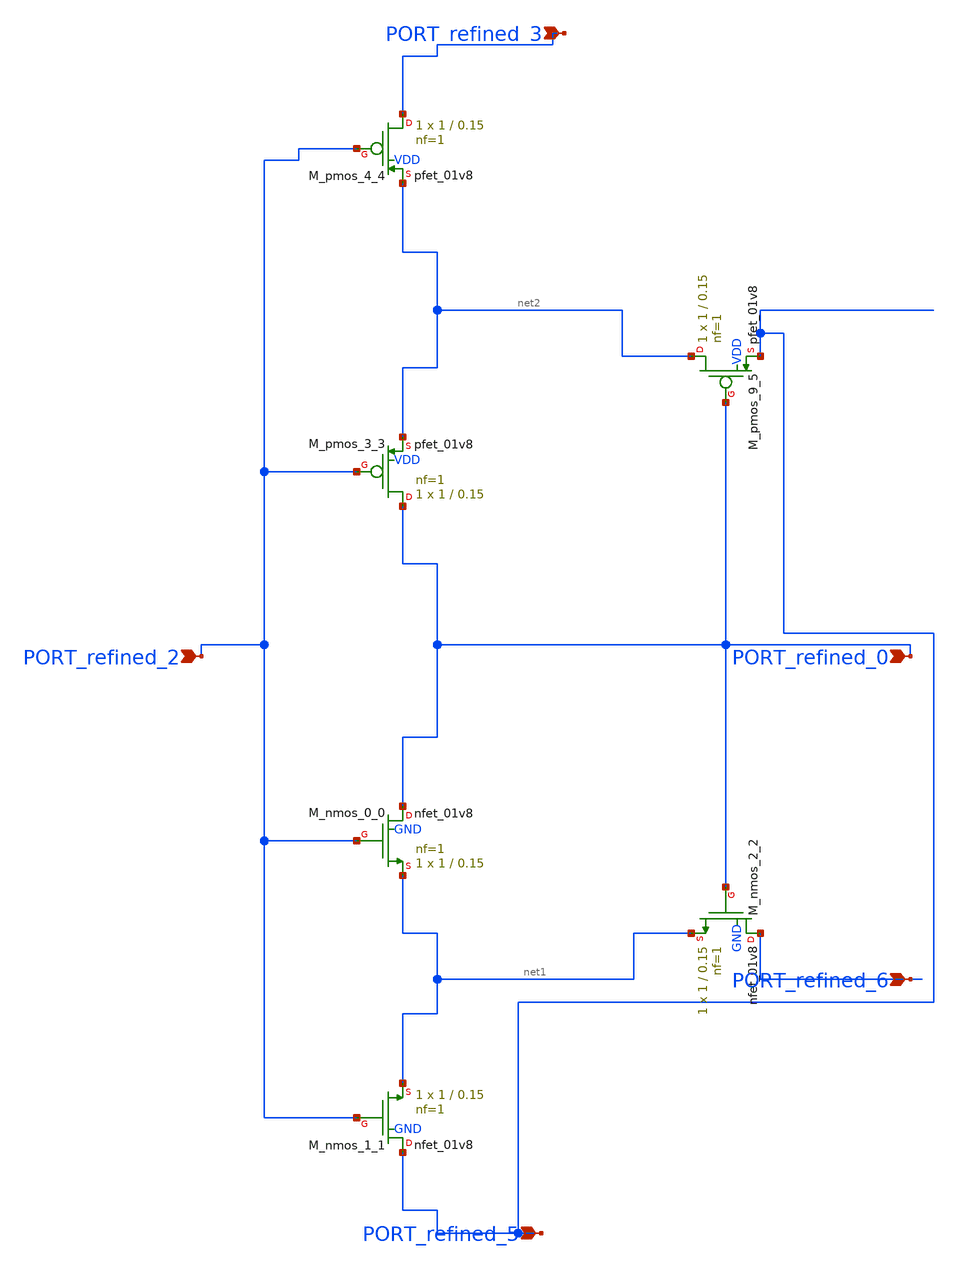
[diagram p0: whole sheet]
** sch_path: schematics/SchemGen/10_1109_ACCESS_2019_2920437_04_003.sch
**.subckt 10_1109_ACCESS_2019_2920437_04_003 PORT_refined_5 PORT_refined_0 PORT_refined_3
*+ PORT_refined_6 PORT_refined_2
*.ipin PORT_refined_5
*.ipin PORT_refined_0
*.ipin PORT_refined_3
*.ipin PORT_refined_6
*.ipin PORT_refined_2
XM_nmos_0_0 PORT_refined_0 PORT_refined_2 net1 GND sky130_fd_pr__nfet_01v8 L=0.15 W=1 nf=1 ad='int((1 + 1)/2) * 1 / 1 * 0.29'
+ as='int((1 + 2)/2) * 1 / 1 * 0.29' pd='2*int((1 + 1)/2) * (1 / 1 + 0.29)' ps='2*int((1 + 2)/2) * (1 / 1 + 0.29)'
+ nrd='0.29 / 1 ' nrs='0.29 / 1 ' sa=0 sb=0 sd=0 mult=1 m=1
XM_nmos_1_1 PORT_refined_5 PORT_refined_2 net1 GND sky130_fd_pr__nfet_01v8 L=0.15 W=1 nf=1 ad='int((1 + 1)/2) * 1 / 1 * 0.29'
+ as='int((1 + 2)/2) * 1 / 1 * 0.29' pd='2*int((1 + 1)/2) * (1 / 1 + 0.29)' ps='2*int((1 + 2)/2) * (1 / 1 + 0.29)'
+ nrd='0.29 / 1 ' nrs='0.29 / 1 ' sa=0 sb=0 sd=0 mult=1 m=1
XM_nmos_2_2 PORT_refined_6 PORT_refined_0 net1 GND sky130_fd_pr__nfet_01v8 L=0.15 W=1 nf=1 ad='int((1 + 1)/2) * 1 / 1 * 0.29'
+ as='int((1 + 2)/2) * 1 / 1 * 0.29' pd='2*int((1 + 1)/2) * (1 / 1 + 0.29)' ps='2*int((1 + 2)/2) * (1 / 1 + 0.29)'
+ nrd='0.29 / 1 ' nrs='0.29 / 1 ' sa=0 sb=0 sd=0 mult=1 m=1
XM_pmos_3_3 PORT_refined_0 PORT_refined_2 net2 VDD sky130_fd_pr__pfet_01v8 L=0.15 W=1 nf=1 ad='int((1 + 1)/2) * 1 / 1 * 0.29'
+ as='int((1 + 2)/2) * 1 / 1 * 0.29' pd='2*int((1 + 1)/2) * (1 / 1 + 0.29)' ps='2*int((1 + 2)/2) * (1 / 1 + 0.29)'
+ nrd='0.29 / 1 ' nrs='0.29 / 1 ' sa=0 sb=0 sd=0 mult=1 m=1
XM_pmos_4_4 PORT_refined_3 PORT_refined_2 net2 VDD sky130_fd_pr__pfet_01v8 L=0.15 W=1 nf=1 ad='int((1 + 1)/2) * 1 / 1 * 0.29'
+ as='int((1 + 2)/2) * 1 / 1 * 0.29' pd='2*int((1 + 1)/2) * (1 / 1 + 0.29)' ps='2*int((1 + 2)/2) * (1 / 1 + 0.29)'
+ nrd='0.29 / 1 ' nrs='0.29 / 1 ' sa=0 sb=0 sd=0 mult=1 m=1
XM_pmos_9_5 net2 PORT_refined_0 PORT_refined_5 VDD sky130_fd_pr__pfet_01v8 L=0.15 W=1 nf=1 ad='int((1 + 1)/2) * 1 / 1 * 0.29'
+ as='int((1 + 2)/2) * 1 / 1 * 0.29' pd='2*int((1 + 1)/2) * (1 / 1 + 0.29)' ps='2*int((1 + 2)/2) * (1 / 1 + 0.29)'
+ nrd='0.29 / 1 ' nrs='0.29 / 1 ' sa=0 sb=0 sd=0 mult=1 m=1
**.ends
.end
